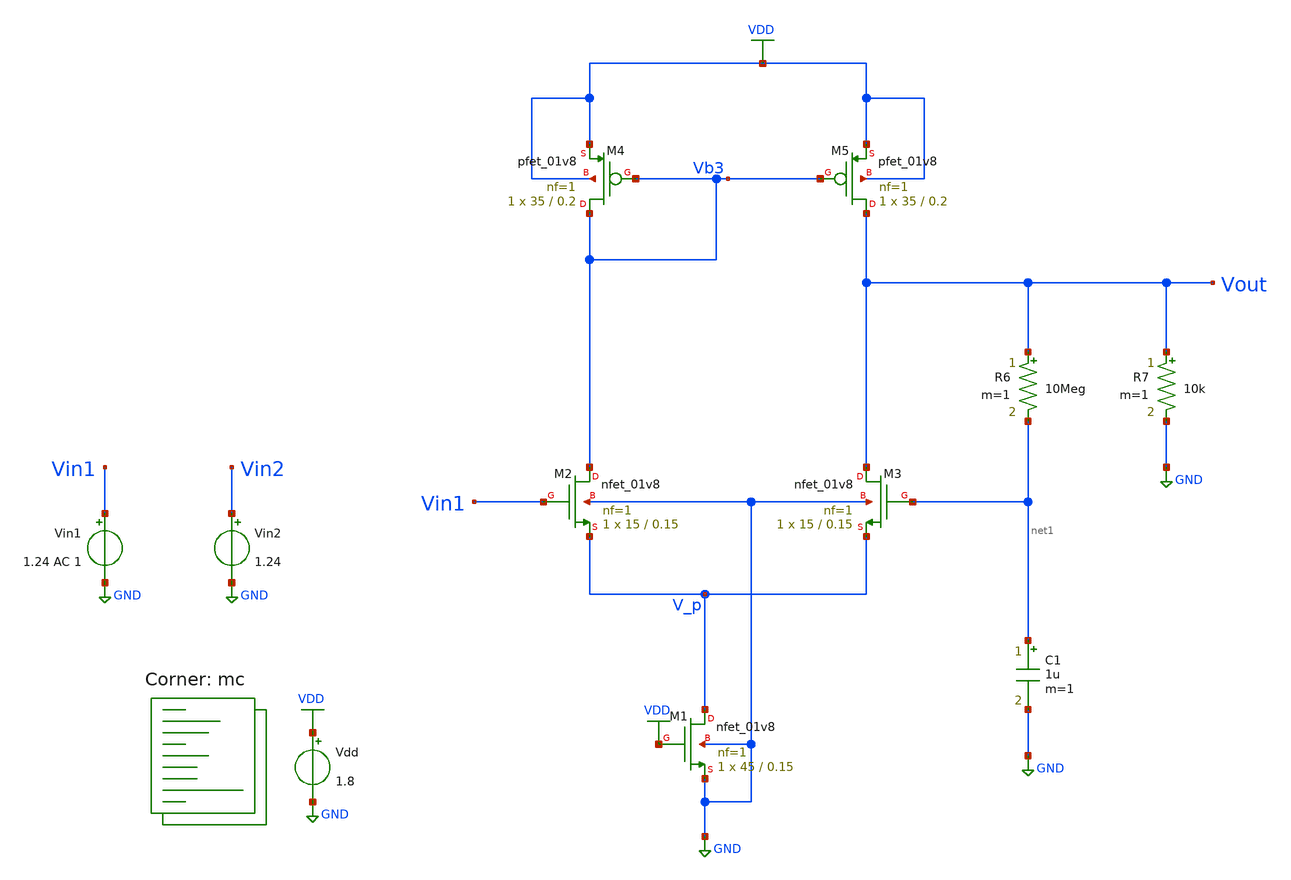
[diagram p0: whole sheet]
** sch_path: projects/montecarlo/xschem_ngspice/inverter/tb_ota_mc.sch
**.subckt tb_ota_mc
Vdd VDD GND 1.8
Vin1 Vin1 GND 1.24 AC 1
Vin2 Vin2 GND 1.24
XM5 Vout Vb3 VDD VDD sky130_fd_pr__pfet_01v8 L=0.2 W=35 nf=1 ad='int((nf+1)/2) * W/nf * 0.29' as='int((nf+2)/2) * W/nf * 0.29'
+ pd='2*int((nf+1)/2) * (W/nf + 0.29)' ps='2*int((nf+2)/2) * (W/nf + 0.29)' nrd='0.29 / W' nrs='0.29 / W'
+ sa=0 sb=0 sd=0 mult=1 m=1
XM4 Vb3 Vb3 VDD VDD sky130_fd_pr__pfet_01v8 L=0.2 W=35 nf=1 ad='int((nf+1)/2) * W/nf * 0.29' as='int((nf+2)/2) * W/nf * 0.29'
+ pd='2*int((nf+1)/2) * (W/nf + 0.29)' ps='2*int((nf+2)/2) * (W/nf + 0.29)' nrd='0.29 / W' nrs='0.29 / W'
+ sa=0 sb=0 sd=0 mult=1 m=1
XM3 Vout net1 V_p GND sky130_fd_pr__nfet_01v8 L=0.15 W=15 nf=1 ad='int((nf+1)/2) * W/nf * 0.29' as='int((nf+2)/2) * W/nf * 0.29'
+ pd='2*int((nf+1)/2) * (W/nf + 0.29)' ps='2*int((nf+2)/2) * (W/nf + 0.29)' nrd='0.29 / W' nrs='0.29 / W'
+ sa=0 sb=0 sd=0 mult=1 m=1
XM2 Vb3 Vin1 V_p GND sky130_fd_pr__nfet_01v8 L=0.15 W=15 nf=1 ad='int((nf+1)/2) * W/nf * 0.29' as='int((nf+2)/2) * W/nf * 0.29'
+ pd='2*int((nf+1)/2) * (W/nf + 0.29)' ps='2*int((nf+2)/2) * (W/nf + 0.29)' nrd='0.29 / W' nrs='0.29 / W'
+ sa=0 sb=0 sd=0 mult=1 m=1
XM1 V_p VDD GND GND sky130_fd_pr__nfet_01v8 L=0.15 W=45 nf=1 ad='int((nf+1)/2) * W/nf * 0.29' as='int((nf+2)/2) * W/nf * 0.29'
+ pd='2*int((nf+1)/2) * (W/nf + 0.29)' ps='2*int((nf+2)/2) * (W/nf + 0.29)' nrd='0.29 / W' nrs='0.29 / W'
+ sa=0 sb=0 sd=0 mult=1 m=1
R6 Vout net1 10Meg m=1
R7 Vout GND 10k m=1
C1 net1 GND 1u m=1
**** begin user architecture code



.option wnflag=1
.option savecurrents
.save @m.xm1.msky130_fd_pr__nfet_01v8[gm] @m.xm1.msky130_fd_pr__nfet_01v8[vth] @m.xm2.msky130_fd_pr__nfet_01v8[gm] @m.xm2.msky130_fd_pr__nfet_01v8[vth] @m.xm3.msky130_fd_pr__nfet_01v8[gm] @m.xm3.msky130_fd_pr__nfet_01v8[vth] @m.xm4.msky130_fd_pr__pfet_01v8[gm] @m.xm4.msky130_fd_pr__pfet_01v8[vth] @m.xm5.msky130_fd_pr__pfet_01v8[gm] @m.xm5.msky130_fd_pr__pfet_01v8[vth] @m.xm6.msky130_fd_pr__nfet_01v8[gm] @m.xm6.msky130_fd_pr__nfet_01v8[vth] @m.xm7.msky130_fd_pr__nfet_01v8[gm] @m.xm7.msky130_fd_pr__nfet_01v8[vth] @m.xm8.msky130_fd_pr__pfet_01v8[gm] @m.xm8.msky130_fd_pr__pfet_01v8[vth] @m.xm9.msky130_fd_pr__pfet_01v8[gm] @m.xm9.msky130_fd_pr__pfet_01v8[vth] @m.xm10.msky130_fd_pr__nfet_01v8[gm] @m.xm10.msky130_fd_pr__nfet_01v8[vth]

.control

  let runs=20
  let run=1

  dowhile run <= runs
    save all
    * dc vin 0 1.8 0.01
    ac dec 20 1 1T
    * tran 1u 3m
    write tb_ota_mc.raw
    set appendwrite
    reset
    let run = run + 1
  end

.endc



.lib $::SKYWATER_MODELS/sky130.lib.spice mc
**** end user architecture code
**.ends
.GLOBAL GND
.GLOBAL VDD
.end
